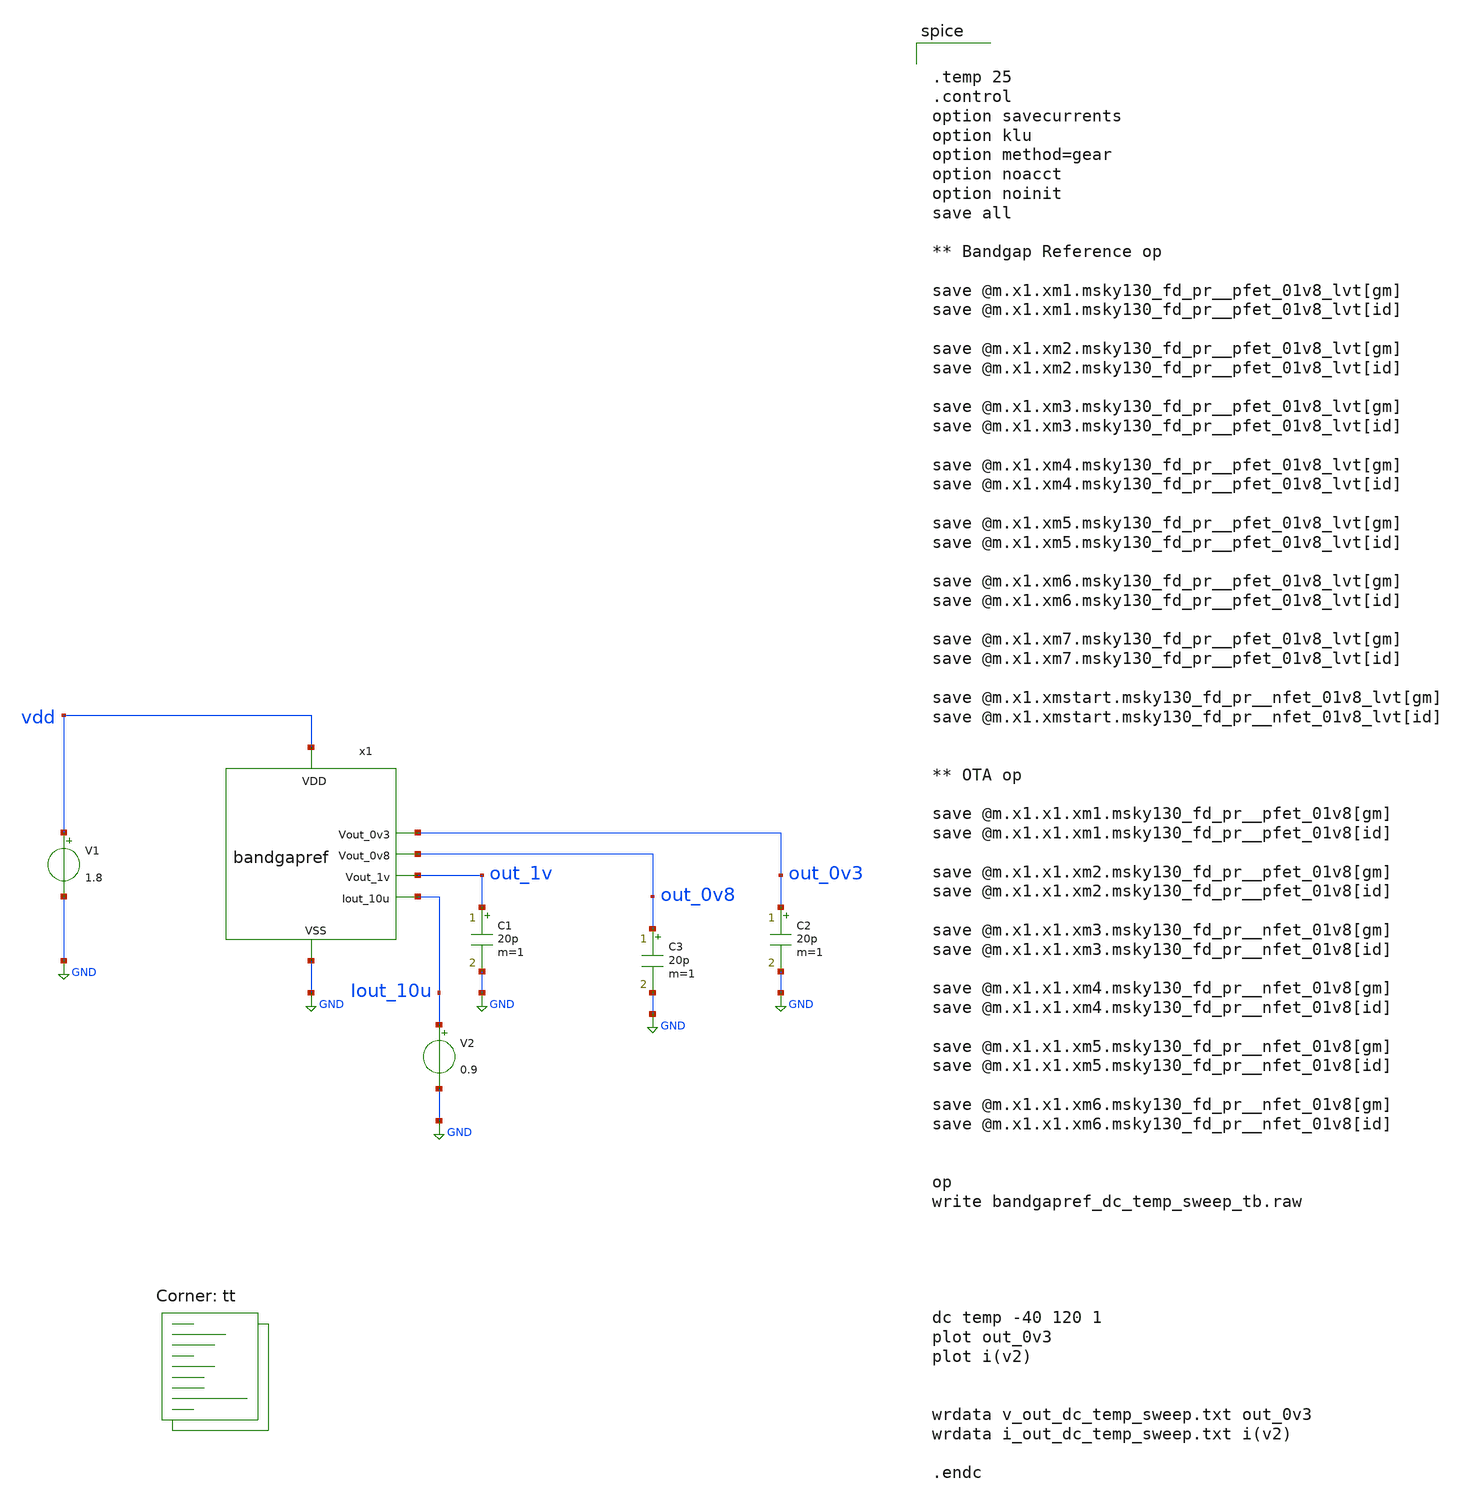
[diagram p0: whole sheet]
** sch_path: xschem/bandgapref_dc_temp_sweep_tb.sch
**.subckt bandgapref_dc_temp_sweep_tb
V1 vdd GND 1.8
.save i(v1)
x1 vdd out_0v3 GND out_1v out_0v8 Iout_10u bandgapref
C1 out_1v GND 20p m=1
C2 out_0v3 GND 20p m=1
C3 out_0v8 GND 20p m=1
V2 Iout_10u GND 0.9
.save i(v2)
**** begin user architecture code
.lib $::SKYWATER_MODELS/sky130.lib.spice tt


.temp 25
.control
option savecurrents
option klu
option method=gear
option noacct
option noinit
save all

** Bandgap Reference op

save @m.x1.xm1.msky130_fd_pr__pfet_01v8_lvt[gm]
save @m.x1.xm1.msky130_fd_pr__pfet_01v8_lvt[id]

save @m.x1.xm2.msky130_fd_pr__pfet_01v8_lvt[gm]
save @m.x1.xm2.msky130_fd_pr__pfet_01v8_lvt[id]

save @m.x1.xm3.msky130_fd_pr__pfet_01v8_lvt[gm]
save @m.x1.xm3.msky130_fd_pr__pfet_01v8_lvt[id]

save @m.x1.xm4.msky130_fd_pr__pfet_01v8_lvt[gm]
save @m.x1.xm4.msky130_fd_pr__pfet_01v8_lvt[id]

save @m.x1.xm5.msky130_fd_pr__pfet_01v8_lvt[gm]
save @m.x1.xm5.msky130_fd_pr__pfet_01v8_lvt[id]

save @m.x1.xm6.msky130_fd_pr__pfet_01v8_lvt[gm]
save @m.x1.xm6.msky130_fd_pr__pfet_01v8_lvt[id]

save @m.x1.xm7.msky130_fd_pr__pfet_01v8_lvt[gm]
save @m.x1.xm7.msky130_fd_pr__pfet_01v8_lvt[id]

save @m.x1.xmstart.msky130_fd_pr__nfet_01v8_lvt[gm]
save @m.x1.xmstart.msky130_fd_pr__nfet_01v8_lvt[id]


** OTA op

save @m.x1.x1.xm1.msky130_fd_pr__pfet_01v8[gm]
save @m.x1.x1.xm1.msky130_fd_pr__pfet_01v8[id]

save @m.x1.x1.xm2.msky130_fd_pr__pfet_01v8[gm]
save @m.x1.x1.xm2.msky130_fd_pr__pfet_01v8[id]

save @m.x1.x1.xm3.msky130_fd_pr__nfet_01v8[gm]
save @m.x1.x1.xm3.msky130_fd_pr__nfet_01v8[id]

save @m.x1.x1.xm4.msky130_fd_pr__nfet_01v8[gm]
save @m.x1.x1.xm4.msky130_fd_pr__nfet_01v8[id]

save @m.x1.x1.xm5.msky130_fd_pr__nfet_01v8[gm]
save @m.x1.x1.xm5.msky130_fd_pr__nfet_01v8[id]

save @m.x1.x1.xm6.msky130_fd_pr__nfet_01v8[gm]
save @m.x1.x1.xm6.msky130_fd_pr__nfet_01v8[id]


op
write bandgapref_dc_temp_sweep_tb.raw





dc temp -40 120 1
plot out_0v3
plot i(v2)


wrdata v_out_dc_temp_sweep.txt out_0v3
wrdata i_out_dc_temp_sweep.txt i(v2)

.endc

**** end user architecture code
**.ends
.GLOBAL GND
.end
